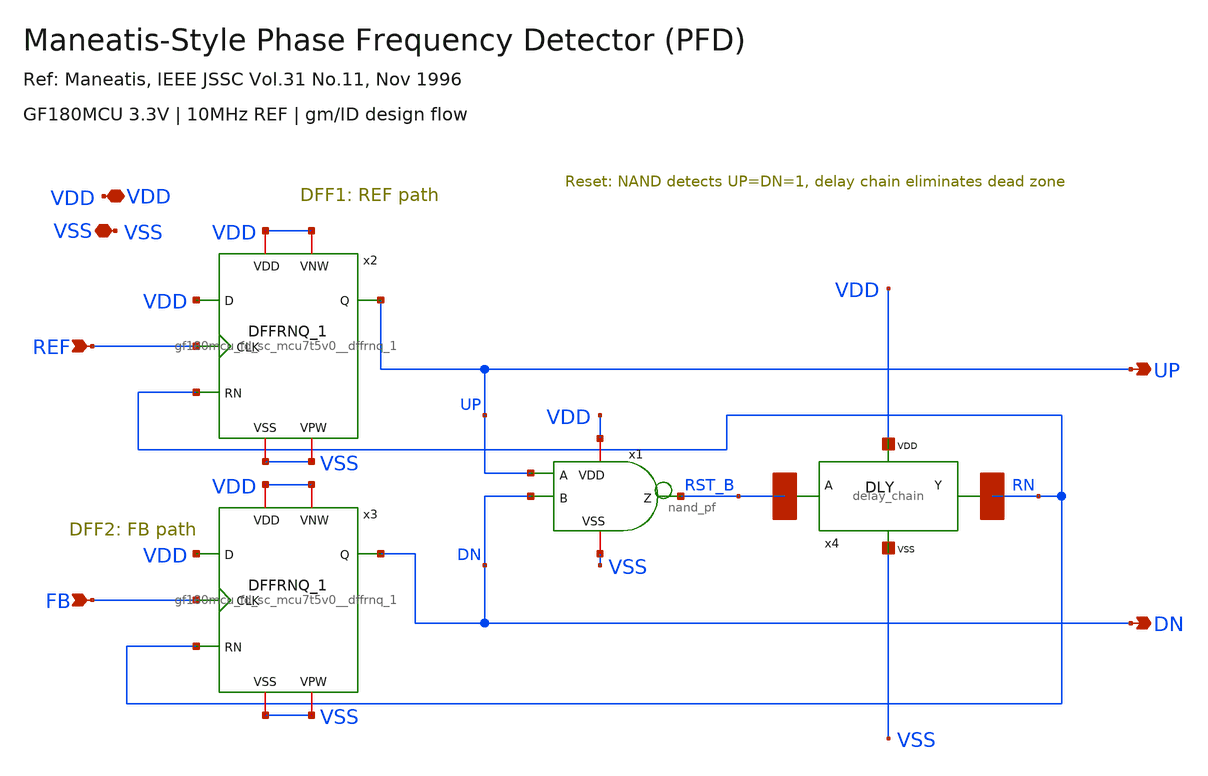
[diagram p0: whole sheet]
** sch_path: designs/libs/core_analog/pfd/leftover_files/pfd.sch
**.subckt pfd REF FB UP DN VDD VSS
*.ipin REF
*.ipin FB
*.opin UP
*.opin DN
*.iopin VDD
*.iopin VSS
x2 VDD RN REF UP VDD VDD VSS VSS gf180mcu_fd_sc_mcu7t5v0__dffrnq_1
x3 VDD RN FB DN VDD VDD VSS VSS gf180mcu_fd_sc_mcu7t5v0__dffrnq_1
x1 VDD RST_B UP DN VSS nand_pf
x4 RST_B RN VDD VSS delay_chain
**.ends
.end
